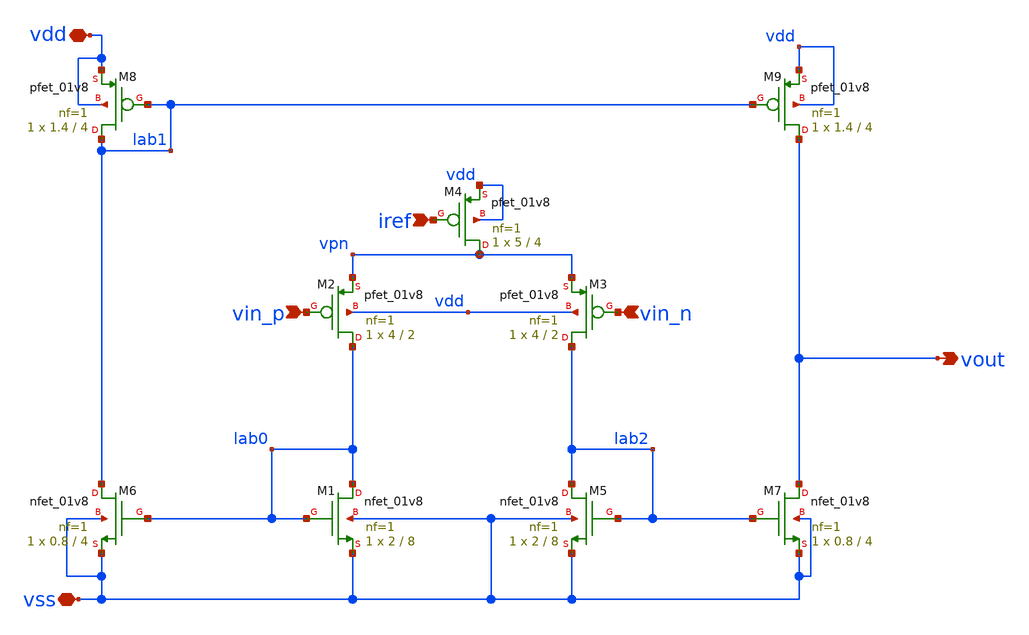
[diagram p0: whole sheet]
** sch_path: design/xschem/low_noise_amp_v1.sch
**.subckt low_noise_amp_v1 iref vin_p vin_n vdd vss vout
*.ipin iref
*.ipin vin_p
*.ipin vin_n
*.iopin vdd
*.iopin vss
*.opin vout
XM1 lab0 lab0 vss vss sky130_fd_pr__nfet_01v8 L=8 W=2 nf=1 ad='W * 0.29' as='W * 0.29' pd='2 * (W + 0.29)'
+ ps='2 * (W + 0.29)' nrd='0.29 / W' nrs='0.29 / W' sa=0 sb=0 sd=0 mult=1 m=1
XM2 lab0 vin_p vpn vdd sky130_fd_pr__pfet_01v8 L=2 W=4 nf=1 ad='W * 0.29' as='W * 0.29' pd='2 * (W + 0.29)'
+ ps='2 * (W + 0.29)' nrd='0.29 / W' nrs='0.29 / W' sa=0 sb=0 sd=0 mult=1 m=1
XM3 lab2 vin_n vpn vdd sky130_fd_pr__pfet_01v8 L=2 W=4 nf=1 ad='W * 0.29' as='W * 0.29' pd='2 * (W + 0.29)'
+ ps='2 * (W + 0.29)' nrd='0.29 / W' nrs='0.29 / W' sa=0 sb=0 sd=0 mult=1 m=1
XM4 vpn iref vdd vdd sky130_fd_pr__pfet_01v8 L=4 W=5 nf=1 ad='W * 0.29' as='W * 0.29' pd='2 * (W + 0.29)'
+ ps='2 * (W + 0.29)' nrd='0.29 / W' nrs='0.29 / W' sa=0 sb=0 sd=0 mult=1 m=1
XM5 lab2 lab2 vss vss sky130_fd_pr__nfet_01v8 L=8 W=2 nf=1 ad='W * 0.29' as='W * 0.29' pd='2 * (W + 0.29)'
+ ps='2 * (W + 0.29)' nrd='0.29 / W' nrs='0.29 / W' sa=0 sb=0 sd=0 mult=1 m=1
XM6 lab1 lab0 vss vss sky130_fd_pr__nfet_01v8 L=4 W=0.8 nf=1 ad='W * 0.29' as='W * 0.29' pd='2 * (W + 0.29)'
+ ps='2 * (W + 0.29)' nrd='0.29 / W' nrs='0.29 / W' sa=0 sb=0 sd=0 mult=1 m=1
XM7 vout lab2 vss vss sky130_fd_pr__nfet_01v8 L=4 W=0.8 nf=1 ad='W * 0.29' as='W * 0.29' pd='2 * (W + 0.29)'
+ ps='2 * (W + 0.29)' nrd='0.29 / W' nrs='0.29 / W' sa=0 sb=0 sd=0 mult=1 m=1
XM8 lab1 lab1 vdd vdd sky130_fd_pr__pfet_01v8 L=4 W=1.4 nf=1 ad='W * 0.29' as='W * 0.29' pd='2 * (W + 0.29)'
+ ps='2 * (W + 0.29)' nrd='0.29 / W' nrs='0.29 / W' sa=0 sb=0 sd=0 mult=1 m=1
XM9 vout lab1 vdd vdd sky130_fd_pr__pfet_01v8 L=4 W=1.4 nf=1 ad='W * 0.29' as='W * 0.29' pd='2 * (W + 0.29)'
+ ps='2 * (W + 0.29)' nrd='0.29 / W' nrs='0.29 / W' sa=0 sb=0 sd=0 mult=1 m=1
**.ends
.end
